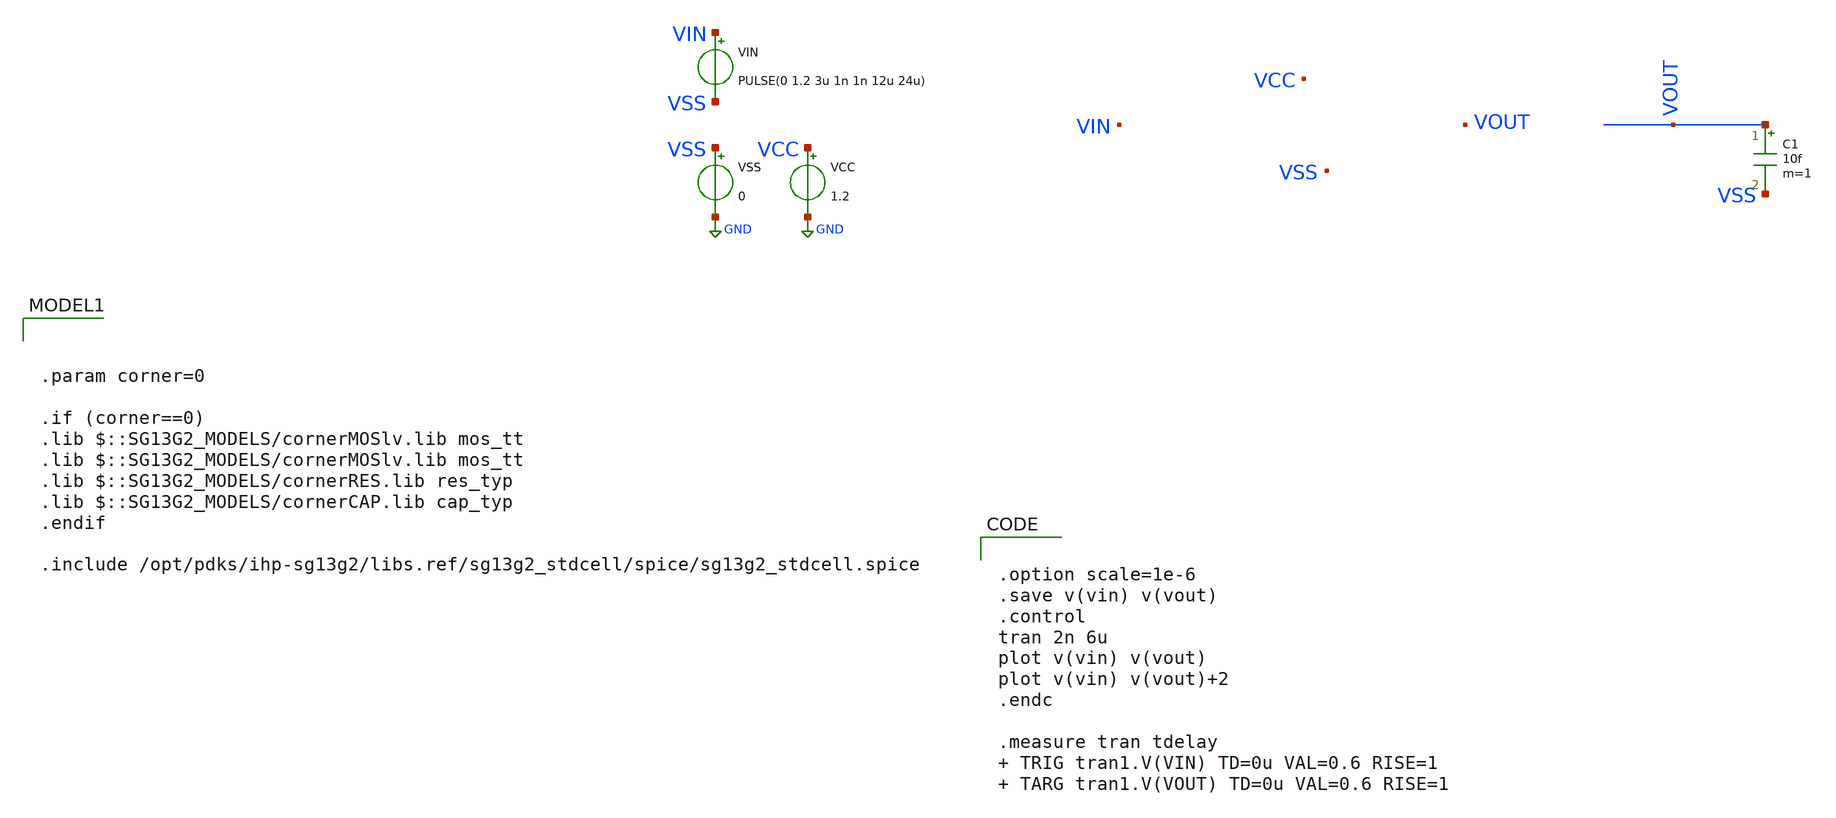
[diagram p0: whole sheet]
** sch_path: tb_delaycell.sch
**.subckt tb_delaycell
VCC VCC GND 1.2
VSS VSS GND 0
VIN VIN VSS PULSE(0 1.2 3u 1n 1n 12u 24u)
C1 VOUT VSS 10f m=1
**** begin user architecture code


.option scale=1e-6
.save v(vin) v(vout)
.control
tran 2n 6u
plot v(vin) v(vout)
plot v(vin) v(vout)+2
.endc

.measure tran tdelay  TRIG tran1.V(VIN) TD=0u VAL=0.6 RISE=1  TARG tran1.V(VOUT) TD=0u VAL=0.6
+ RISE=1






.param corner=0

.if (corner==0)
.lib $::SG13G2_MODELS/cornerMOSlv.lib mos_tt
.lib $::SG13G2_MODELS/cornerMOSlv.lib mos_tt
.lib $::SG13G2_MODELS/cornerRES.lib res_typ
.lib $::SG13G2_MODELS/cornerCAP.lib cap_typ
.endif

.include /opt/pdks/ihp-sg13g2/libs.ref/sg13g2_stdcell/spice/sg13g2_stdcell.spice

**** end user architecture code
**.ends
.GLOBAL GND
.end
